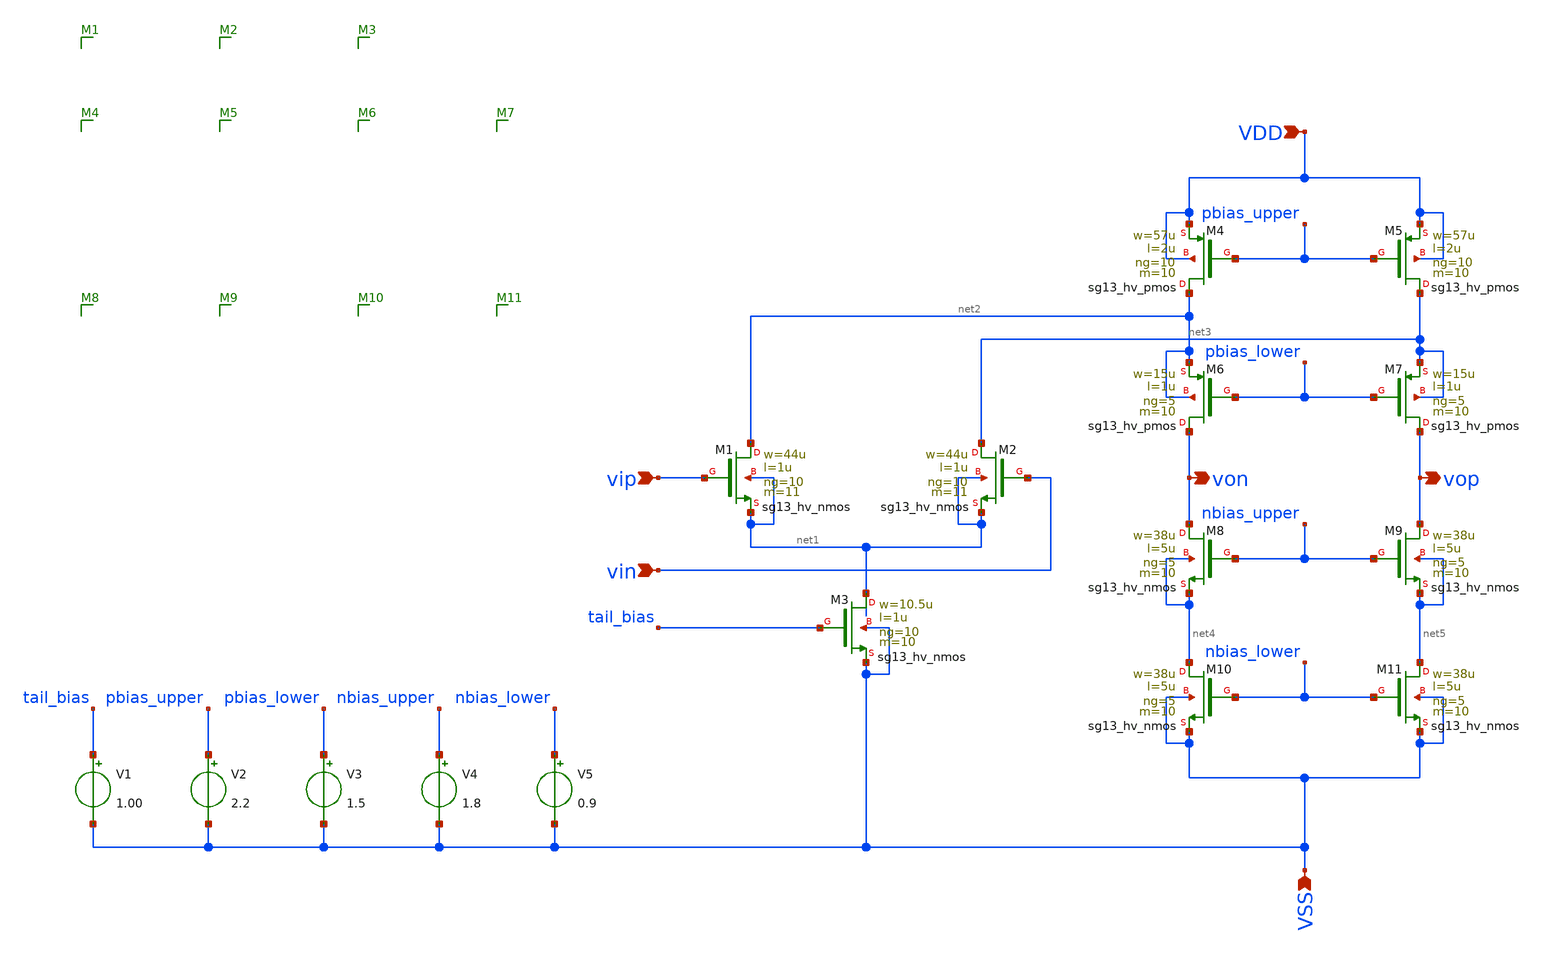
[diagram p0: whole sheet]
** sch_path: schematic/folded_cascode.sch
**.subckt folded_cascode VDD vip vin vop von VSS
*.ipin VDD
*.ipin vip
*.ipin vin
*.opin vop
*.opin von
*.ipin VSS
XM1 net2 vip net1 net1 sg13_hv_nmos w=44u l=1u ng=10 m=11 mm_ok=1
XM4 net2 pbias_upper VDD VDD sg13_hv_pmos w=57u l=2u ng=10 m=10 mm_ok=1
XM2 net3 vin net1 net1 sg13_hv_nmos w=44u l=1u ng=10 m=11 mm_ok=1
XM3 net1 tail_bias VSS VSS sg13_hv_nmos w=10.5u l=1u ng=10 m=10 mm_ok=1
XM5 net3 pbias_upper VDD VDD sg13_hv_pmos w=57u l=2u ng=10 m=10 mm_ok=1
XM6 von pbias_lower net2 net2 sg13_hv_pmos w=15u l=1u ng=5 m=10 mm_ok=1
XM7 vop pbias_lower net3 net3 sg13_hv_pmos w=15u l=1u ng=5 m=10 mm_ok=1
XM9 vop nbias_upper net5 net5 sg13_hv_nmos w=38u l=5u ng=5 m=10 mm_ok=1
XM8 von nbias_upper net4 net4 sg13_hv_nmos w=38u l=5u ng=5 m=10 mm_ok=1
XM11 net5 nbias_lower VSS VSS sg13_hv_nmos w=38u l=5u ng=5 m=10 mm_ok=1
XM10 net4 nbias_lower VSS VSS sg13_hv_nmos w=38u l=5u ng=5 m=10 mm_ok=1
V1 tail_bias VSS 1.00
V2 pbias_upper VSS 2.2
V3 pbias_lower VSS 1.5
V4 nbias_upper VSS 1.8
V5 nbias_lower VSS 0.9
**.ends
.end
